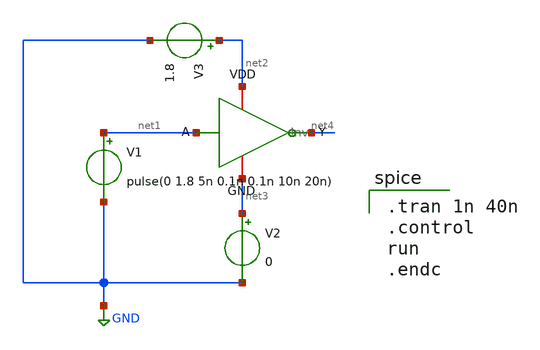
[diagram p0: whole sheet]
** sch_path: Inv_Test.sch
**.subckt Inv_Test
V1 net1 GND pulse(0 1.8 5n 0.1n 0.1n 10n 20n)
V2 net3 GND 0
V3 net2 GND 1.8
x1 net2 net1 net4 net3 Inv
**** begin user architecture code
 .lib $::SKYWATER_MODELS/sky130.lib.spice tt

.tran 1n 40n
.control
run
.endc

**** end user architecture code
**.ends

* expanding   symbol:  workspace/FinalProj/Inv.sym # of pins=4
** sym_path: Inv.sym
** sch_path: Inv.sch
.subckt Inv VDD A Y GND
*.ipin A
*.iopin GND
*.iopin VDD
*.opin Y
XM1 Y A VDD VDD sky130_fd_pr__pfet_01v8 L=0.5 W=1 nf=1 ad='int((nf+1)/2) * W/nf * 0.29' as='int((nf+2)/2) * W/nf * 0.29'
+ pd='2*int((nf+1)/2) * (W/nf + 0.29)' ps='2*int((nf+2)/2) * (W/nf + 0.29)' nrd='0.29 / W' nrs='0.29 / W'
+ sa=0 sb=0 sd=0 mult=1 m=1
XM2 Y A GND GND sky130_fd_pr__nfet_01v8 L=0.5 W=0.5 nf=1 ad='int((nf+1)/2) * W/nf * 0.29' as='int((nf+2)/2) * W/nf * 0.29'
+ pd='2*int((nf+1)/2) * (W/nf + 0.29)' ps='2*int((nf+2)/2) * (W/nf + 0.29)' nrd='0.29 / W' nrs='0.29 / W'
+ sa=0 sb=0 sd=0 mult=1 m=1
.ends

.GLOBAL GND
.end
